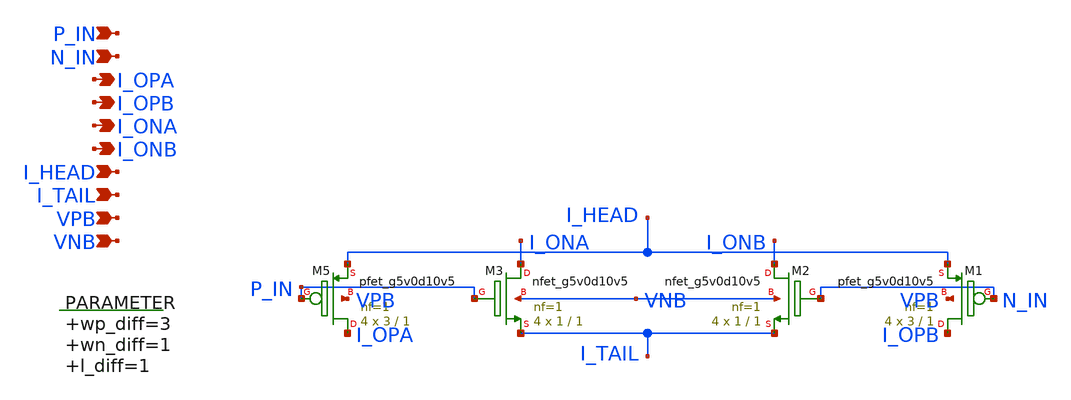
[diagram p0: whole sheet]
** sch_path: xschem/diff_pair.sch
**.subckt diff_pair I_OPA I_OPB P_IN N_IN I_ONA I_ONB I_HEAD I_TAIL VPB VNB
*.opin I_OPA
*.opin I_OPB
*.ipin P_IN
*.ipin N_IN
*.opin I_ONA
*.opin I_ONB
*.ipin I_HEAD
*.ipin I_TAIL
*.ipin VPB
*.ipin VNB
.param wp_diff=3 wn_diff=1 l_diff=1

XM5 I_OPA P_IN I_HEAD VPB sky130_fd_pr__pfet_g5v0d10v5 L=1 W=3 nf=1 ad='int((nf+1)/2) * W/nf * 0.29'
+ as='int((nf+2)/2) * W/nf * 0.29' pd='2*int((nf+1)/2) * (W/nf + 0.29)' ps='2*int((nf+2)/2) * (W/nf + 0.29)'
+ nrd='0.29 / W' nrs='0.29 / W' sa=0 sb=0 sd=0 mult=4 m=4
XM1 I_OPB N_IN I_HEAD VPB sky130_fd_pr__pfet_g5v0d10v5 L=1 W=3 nf=1 ad='int((nf+1)/2) * W/nf * 0.29'
+ as='int((nf+2)/2) * W/nf * 0.29' pd='2*int((nf+1)/2) * (W/nf + 0.29)' ps='2*int((nf+2)/2) * (W/nf + 0.29)'
+ nrd='0.29 / W' nrs='0.29 / W' sa=0 sb=0 sd=0 mult=4 m=4
XM3 I_ONA P_IN I_TAIL VNB sky130_fd_pr__nfet_g5v0d10v5 L=1 W=1 nf=1 ad='int((nf+1)/2) * W/nf * 0.29'
+ as='int((nf+2)/2) * W/nf * 0.29' pd='2*int((nf+1)/2) * (W/nf + 0.29)' ps='2*int((nf+2)/2) * (W/nf + 0.29)'
+ nrd='0.29 / W' nrs='0.29 / W' sa=0 sb=0 sd=0 mult=4 m=4
XM2 I_ONB N_IN I_TAIL VNB sky130_fd_pr__nfet_g5v0d10v5 L=1 W=1 nf=1 ad='int((nf+1)/2) * W/nf * 0.29'
+ as='int((nf+2)/2) * W/nf * 0.29' pd='2*int((nf+1)/2) * (W/nf + 0.29)' ps='2*int((nf+2)/2) * (W/nf + 0.29)'
+ nrd='0.29 / W' nrs='0.29 / W' sa=0 sb=0 sd=0 mult=4 m=4
**.ends
.end
